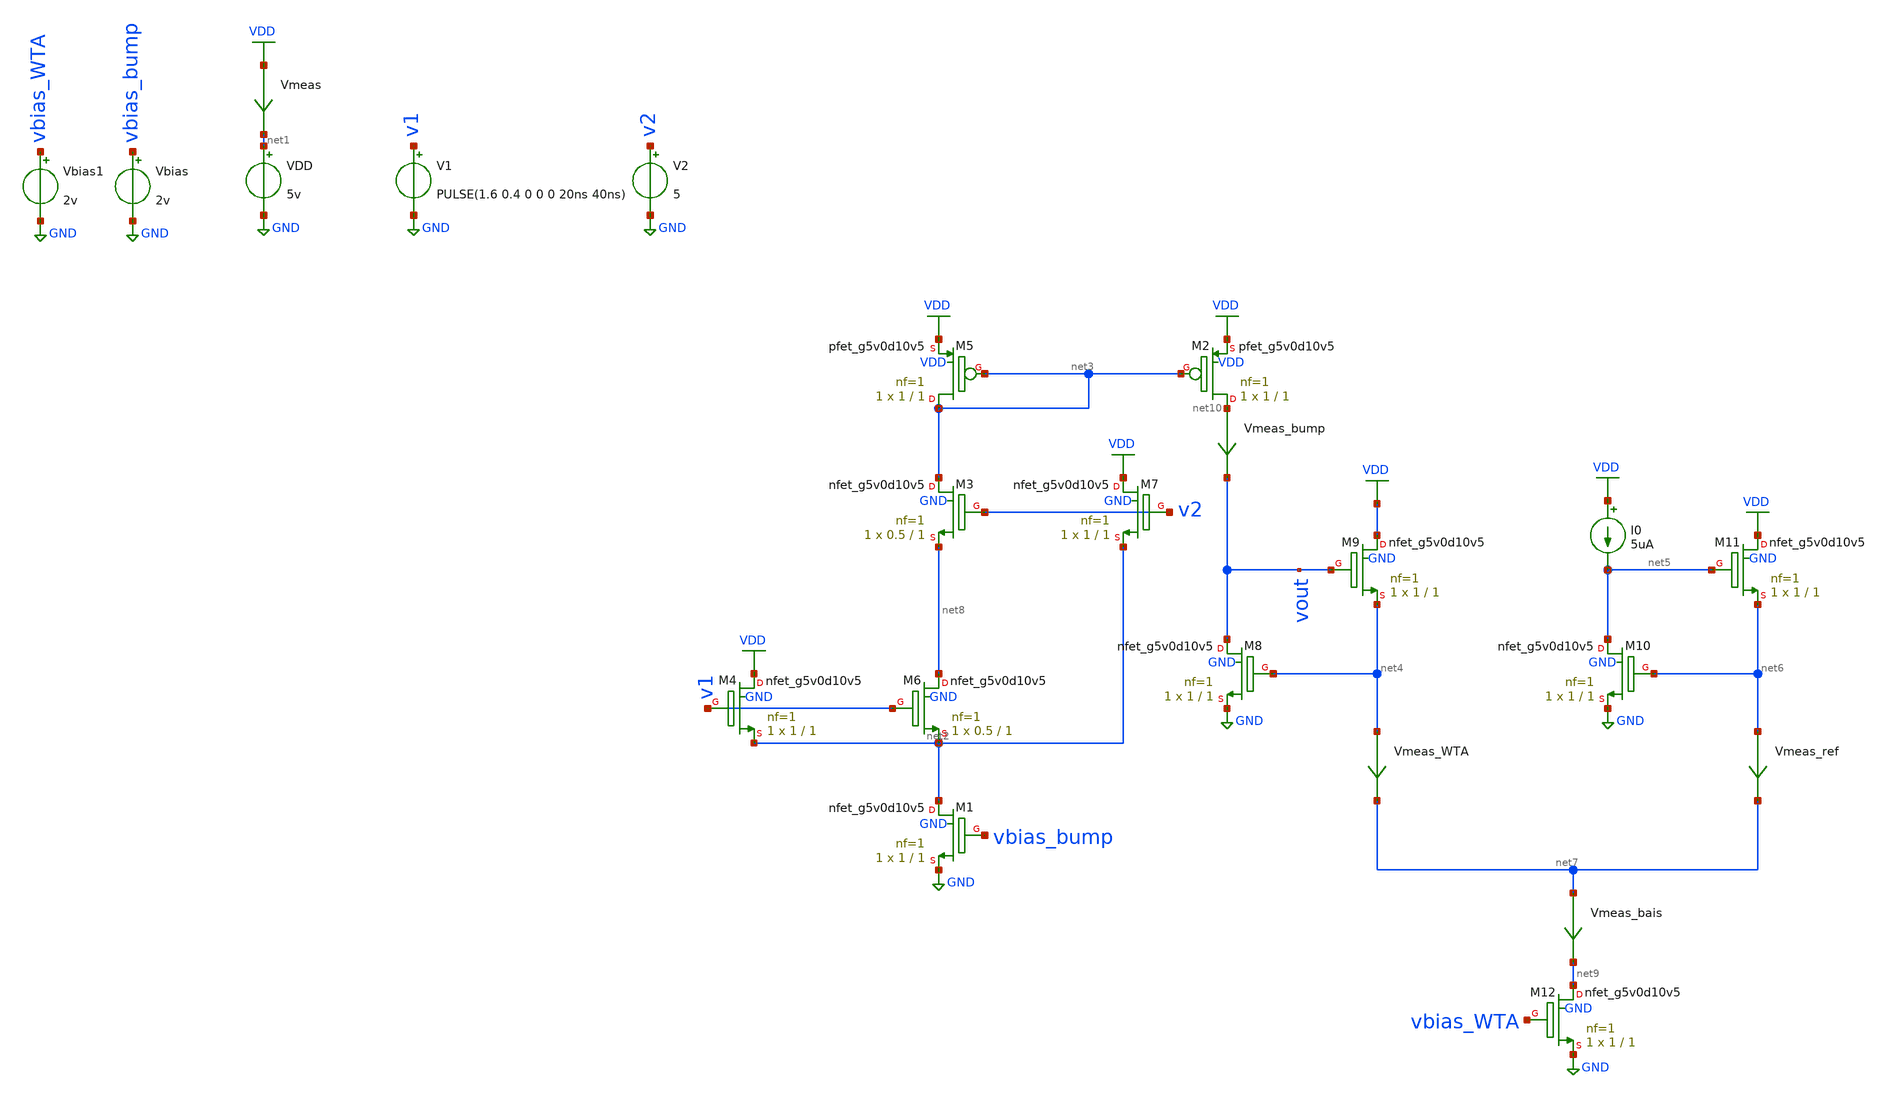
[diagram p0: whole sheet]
** sch_path: schematics/bump_tb.sch
**.subckt bump_tb
Vbias vbias_bump GND 2v
VDD net1 GND 5v
V1 v1 GND PULSE(1.6 0.4 0 0 0 20ns 40ns)
Vmeas VDD net1 0
.save i(vmeas)
Vbias1 vbias_WTA GND 2v
XM3 net3 v2 net8 GND sky130_fd_pr__nfet_g5v0d10v5 L=1 W=0.5 nf=1 ad='int((nf+1)/2) * W/nf * 0.29' as='int((nf+2)/2) * W/nf * 0.29'
+ pd='2*int((nf+1)/2) * (W/nf + 0.29)' ps='2*int((nf+2)/2) * (W/nf + 0.29)' nrd='0.29 / W' nrs='0.29 / W'
+ sa=0 sb=0 sd=0 mult=1 m=1
XM4 VDD v1 net2 GND sky130_fd_pr__nfet_g5v0d10v5 L=1 W=1 nf=1 ad='int((nf+1)/2) * W/nf * 0.29' as='int((nf+2)/2) * W/nf * 0.29'
+ pd='2*int((nf+1)/2) * (W/nf + 0.29)' ps='2*int((nf+2)/2) * (W/nf + 0.29)' nrd='0.29 / W' nrs='0.29 / W'
+ sa=0 sb=0 sd=0 mult=1 m=1
XM6 net8 v1 net2 GND sky130_fd_pr__nfet_g5v0d10v5 L=1 W=0.5 nf=1 ad='int((nf+1)/2) * W/nf * 0.29' as='int((nf+2)/2) * W/nf * 0.29'
+ pd='2*int((nf+1)/2) * (W/nf + 0.29)' ps='2*int((nf+2)/2) * (W/nf + 0.29)' nrd='0.29 / W' nrs='0.29 / W'
+ sa=0 sb=0 sd=0 mult=1 m=1
XM7 VDD v2 net2 GND sky130_fd_pr__nfet_g5v0d10v5 L=1 W=1 nf=1 ad='int((nf+1)/2) * W/nf * 0.29' as='int((nf+2)/2) * W/nf * 0.29'
+ pd='2*int((nf+1)/2) * (W/nf + 0.29)' ps='2*int((nf+2)/2) * (W/nf + 0.29)' nrd='0.29 / W' nrs='0.29 / W'
+ sa=0 sb=0 sd=0 mult=1 m=1
XM1 net2 vbias_bump GND GND sky130_fd_pr__nfet_g5v0d10v5 L=1 W=1 nf=1 ad='int((nf+1)/2) * W/nf * 0.29'
+ as='int((nf+2)/2) * W/nf * 0.29' pd='2*int((nf+1)/2) * (W/nf + 0.29)' ps='2*int((nf+2)/2) * (W/nf + 0.29)'
+ nrd='0.29 / W' nrs='0.29 / W' sa=0 sb=0 sd=0 mult=1 m=1
XM2 net10 net3 VDD VDD sky130_fd_pr__pfet_g5v0d10v5 L=1 W=1 nf=1 ad='int((nf+1)/2) * W/nf * 0.29' as='int((nf+2)/2) * W/nf * 0.29'
+ pd='2*int((nf+1)/2) * (W/nf + 0.29)' ps='2*int((nf+2)/2) * (W/nf + 0.29)' nrd='0.29 / W' nrs='0.29 / W'
+ sa=0 sb=0 sd=0 mult=1 m=1
XM5 net3 net3 VDD VDD sky130_fd_pr__pfet_g5v0d10v5 L=1 W=1 nf=1 ad='int((nf+1)/2) * W/nf * 0.29' as='int((nf+2)/2) * W/nf * 0.29'
+ pd='2*int((nf+1)/2) * (W/nf + 0.29)' ps='2*int((nf+2)/2) * (W/nf + 0.29)' nrd='0.29 / W' nrs='0.29 / W'
+ sa=0 sb=0 sd=0 mult=1 m=1
Vmeas_bump net10 vout 0
.save i(vmeas_bump)
XM8 vout net4 GND GND sky130_fd_pr__nfet_g5v0d10v5 L=1 W=1 nf=1 ad='int((nf+1)/2) * W/nf * 0.29' as='int((nf+2)/2) * W/nf * 0.29'
+ pd='2*int((nf+1)/2) * (W/nf + 0.29)' ps='2*int((nf+2)/2) * (W/nf + 0.29)' nrd='0.29 / W' nrs='0.29 / W'
+ sa=0 sb=0 sd=0 mult=1 m=1
XM9 VDD vout net4 GND sky130_fd_pr__nfet_g5v0d10v5 L=1 W=1 nf=1 ad='int((nf+1)/2) * W/nf * 0.29' as='int((nf+2)/2) * W/nf * 0.29'
+ pd='2*int((nf+1)/2) * (W/nf + 0.29)' ps='2*int((nf+2)/2) * (W/nf + 0.29)' nrd='0.29 / W' nrs='0.29 / W'
+ sa=0 sb=0 sd=0 mult=1 m=1
XM10 net5 net6 GND GND sky130_fd_pr__nfet_g5v0d10v5 L=1 W=1 nf=1 ad='int((nf+1)/2) * W/nf * 0.29' as='int((nf+2)/2) * W/nf * 0.29'
+ pd='2*int((nf+1)/2) * (W/nf + 0.29)' ps='2*int((nf+2)/2) * (W/nf + 0.29)' nrd='0.29 / W' nrs='0.29 / W'
+ sa=0 sb=0 sd=0 mult=1 m=1
XM11 VDD net5 net6 GND sky130_fd_pr__nfet_g5v0d10v5 L=1 W=1 nf=1 ad='int((nf+1)/2) * W/nf * 0.29' as='int((nf+2)/2) * W/nf * 0.29'
+ pd='2*int((nf+1)/2) * (W/nf + 0.29)' ps='2*int((nf+2)/2) * (W/nf + 0.29)' nrd='0.29 / W' nrs='0.29 / W'
+ sa=0 sb=0 sd=0 mult=1 m=1
I0 VDD net5 5uA
XM12 net9 vbias_WTA GND GND sky130_fd_pr__nfet_g5v0d10v5 L=1 W=1 nf=1 ad='int((nf+1)/2) * W/nf * 0.29'
+ as='int((nf+2)/2) * W/nf * 0.29' pd='2*int((nf+1)/2) * (W/nf + 0.29)' ps='2*int((nf+2)/2) * (W/nf + 0.29)'
+ nrd='0.29 / W' nrs='0.29 / W' sa=0 sb=0 sd=0 mult=1 m=1
Vmeas_WTA net4 net7 0
.save i(vmeas_wta)
Vmeas_ref net6 net7 0
.save i(vmeas_ref)
Vmeas_bais net7 net9 0
.save i(vmeas_bais)
V2 v2 GND 5
**** begin user architecture code


.control
save all

dc V1 0 10 0.01
plot i(Vmeas_bump) vs v(v1)-v(v2)
plot v(vout)
plot v(v1)
plot i(Vmeas_bump)
.endc


 .lib $::SKYWATER_MODELS/models/sky130.lib.spice tt

.param mc_mm_switch=0
.param mc_pr_switch=1

**** end user architecture code
**.ends
.GLOBAL GND
.GLOBAL VDD
.end
